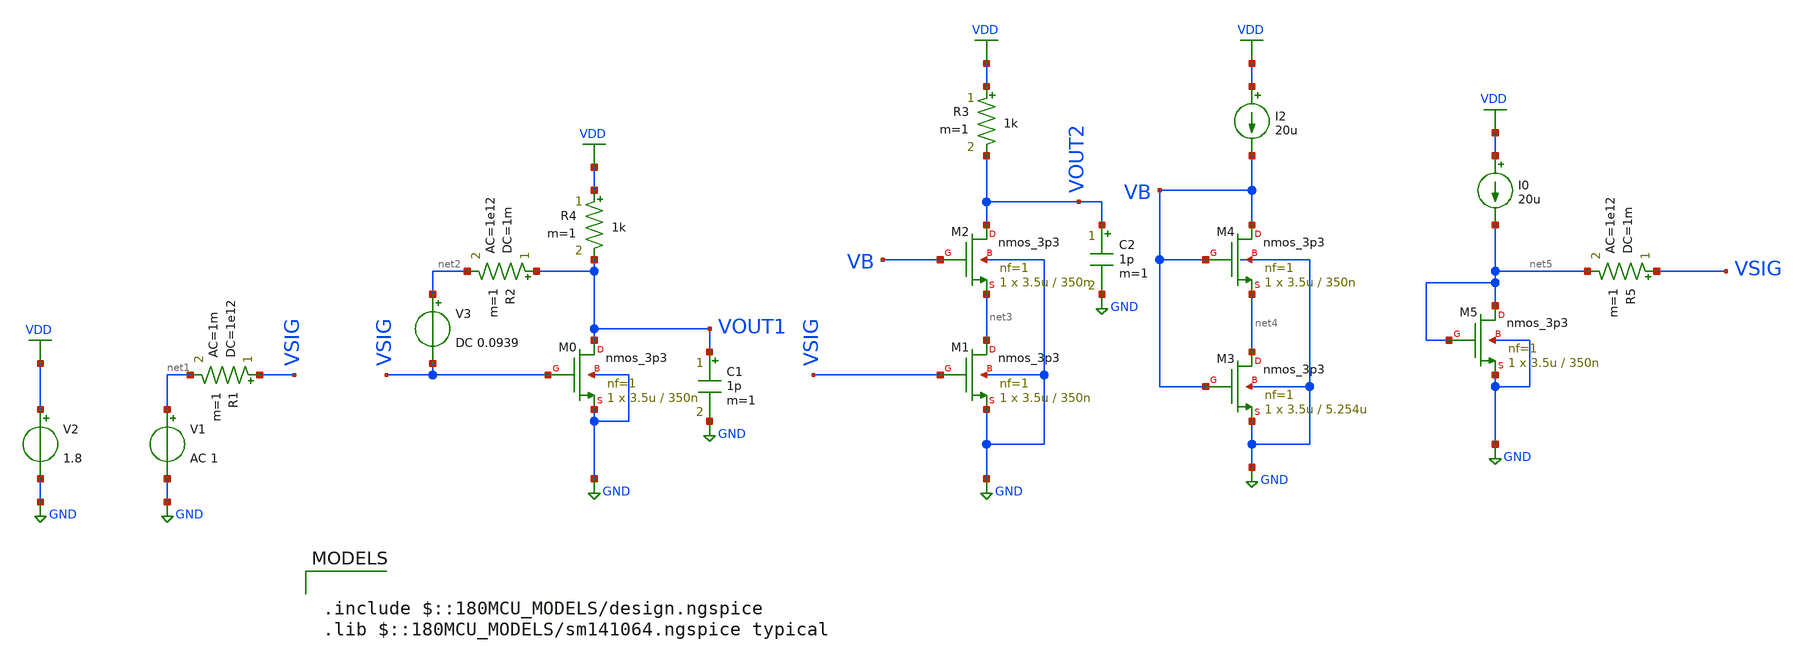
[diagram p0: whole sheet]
** sch_path: ITI_Labs/Lab3/Design/Lab03_bw.sch
**.subckt Lab03_bw
V1 net1 GND AC 1
R1 VSIG net1 1e12 ac=1m m=1
XM0 VOUT1 VSIG GND GND nmos_3p3 L=350n W=3.5u nf=1 ad='int((nf+1)/2) * W/nf * 0.18u' as='int((nf+2)/2) * W/nf * 0.18u'
+ pd='2*int((nf+1)/2) * (W/nf + 0.18u)' ps='2*int((nf+2)/2) * (W/nf + 0.18u)' nrd='0.18u / W' nrs='0.18u / W'
+ sa=0 sb=0 sd=0 m=1
C1 VOUT1 GND 1p m=1
V2 VDD GND 1.8
V3 net2 VSIG DC 0.0939
R2 VOUT1 net2 1m ac=1e12 m=1
XM1 net3 VSIG GND GND nmos_3p3 L=350n W=3.5u nf=1 ad='int((nf+1)/2) * W/nf * 0.18u' as='int((nf+2)/2) * W/nf * 0.18u'
+ pd='2*int((nf+1)/2) * (W/nf + 0.18u)' ps='2*int((nf+2)/2) * (W/nf + 0.18u)' nrd='0.18u / W' nrs='0.18u / W'
+ sa=0 sb=0 sd=0 m=1
XM2 VOUT2 VB net3 GND nmos_3p3 L=350n W=3.5u nf=1 ad='int((nf+1)/2) * W/nf * 0.18u' as='int((nf+2)/2) * W/nf * 0.18u'
+ pd='2*int((nf+1)/2) * (W/nf + 0.18u)' ps='2*int((nf+2)/2) * (W/nf + 0.18u)' nrd='0.18u / W' nrs='0.18u / W'
+ sa=0 sb=0 sd=0 m=1
C2 VOUT2 GND 1p m=1
XM4 VB VB net4 GND nmos_3p3 L=350n W=3.5u nf=1 ad='int((nf+1)/2) * W/nf * 0.18u' as='int((nf+2)/2) * W/nf * 0.18u'
+ pd='2*int((nf+1)/2) * (W/nf + 0.18u)' ps='2*int((nf+2)/2) * (W/nf + 0.18u)' nrd='0.18u / W' nrs='0.18u / W'
+ sa=0 sb=0 sd=0 m=1
I2 VDD VB 20u
XM3 net4 VB GND GND nmos_3p3 L=5.254u W=3.5u nf=1 ad='int((nf+1)/2) * W/nf * 0.18u' as='int((nf+2)/2) * W/nf * 0.18u'
+ pd='2*int((nf+1)/2) * (W/nf + 0.18u)' ps='2*int((nf+2)/2) * (W/nf + 0.18u)' nrd='0.18u / W' nrs='0.18u / W'
+ sa=0 sb=0 sd=0 m=1
R4 VDD VOUT1 1k m=1
R3 VDD VOUT2 1k m=1
XM5 net5 net5 GND GND nmos_3p3 L=350n W=3.5u nf=1 ad='int((nf+1)/2) * W/nf * 0.18u' as='int((nf+2)/2) * W/nf * 0.18u'
+ pd='2*int((nf+1)/2) * (W/nf + 0.18u)' ps='2*int((nf+2)/2) * (W/nf + 0.18u)' nrd='0.18u / W' nrs='0.18u / W'
+ sa=0 sb=0 sd=0 m=1
I0 VDD net5 20u
R5 VSIG net5 1m ac=1e12 m=1
**** begin user architecture code

.include $::180MCU_MODELS/design.ngspice
.lib $::180MCU_MODELS/sm141064.ngspice typical



.control
save all  @m.xm0.m0[id]  @m.xm0.m0[vgs]  @m.xm0.m0[vds]  @m.xm0.m0[vth]  @m.xm0.m0[vdsat]
+  @m.xm0.m0[gm]  @m.xm0.m0[gds]  @m.xm0.m0[gmbs]  @m.xm0.m0[cdb]  @m.xm0.m0[cgd]  @m.xm0.m0[cgs]  @m.xm0.m0[csb]
  @m.xm1.m0[id]  @m.xm1.m0[vgs]  @m.xm1.m0[vds]  @m.xm1.m0[vth]  @m.xm1.m0[vdsat]  @m.xm1.m0[gm]
+  @m.xm1.m0[gds]  @m.xm1.m0[gmbs]  @m.xm1.m0[cdb]  @m.xm1.m0[cgd]  @m.xm1.m0[cgs]  @m.xm1.m0[csb]

  @m.xm2.m0[id]  @m.xm2.m0[vgs]  @m.xm2.m0[vds]  @m.xm2.m0[vth]  @m.xm2.m0[vdsat]  @m.xm2.m0[gm]
+  @m.xm2.m0[gds]  @m.xm2.m0[gmbs]  @m.xm2.m0[cdb]  @m.xm2.m0[cgd]  @m.xm2.m0[cgs]  @m.xm2.m0[csb]

  @m.xm3.m0[id]  @m.xm3.m0[vgs]  @m.xm3.m0[vds]  @m.xm3.m0[vth]  @m.xm3.m0[vdsat]  @m.xm3.m0[gm]
+  @m.xm3.m0[gds]  @m.xm3.m0[gmbs]  @m.xm3.m0[cdb]  @m.xm3.m0[cgd]  @m.xm3.m0[cgs]  @m.xm3.m0[csb]
  @m.xm4.m0[id]  @m.xm4.m0[vgs]  @m.xm4.m0[vds]  @m.xm4.m0[vth]  @m.xm4.m0[vdsat]  @m.xm4.m0[gm]
+  @m.xm4.m0[gds]  @m.xm4.m0[gmbs]  @m.xm4.m0[cdb]  @m.xm4.m0[cgd]  @m.xm4.m0[cgs]  @m.xm4.m0[csb]

*op
*print all > op_point.csv
ac dec 10 1 10g
set appendwrite
remzerovec
write Lab03.raw
.endc


**** end user architecture code
**.ends
.GLOBAL GND
.GLOBAL VDD
.end
